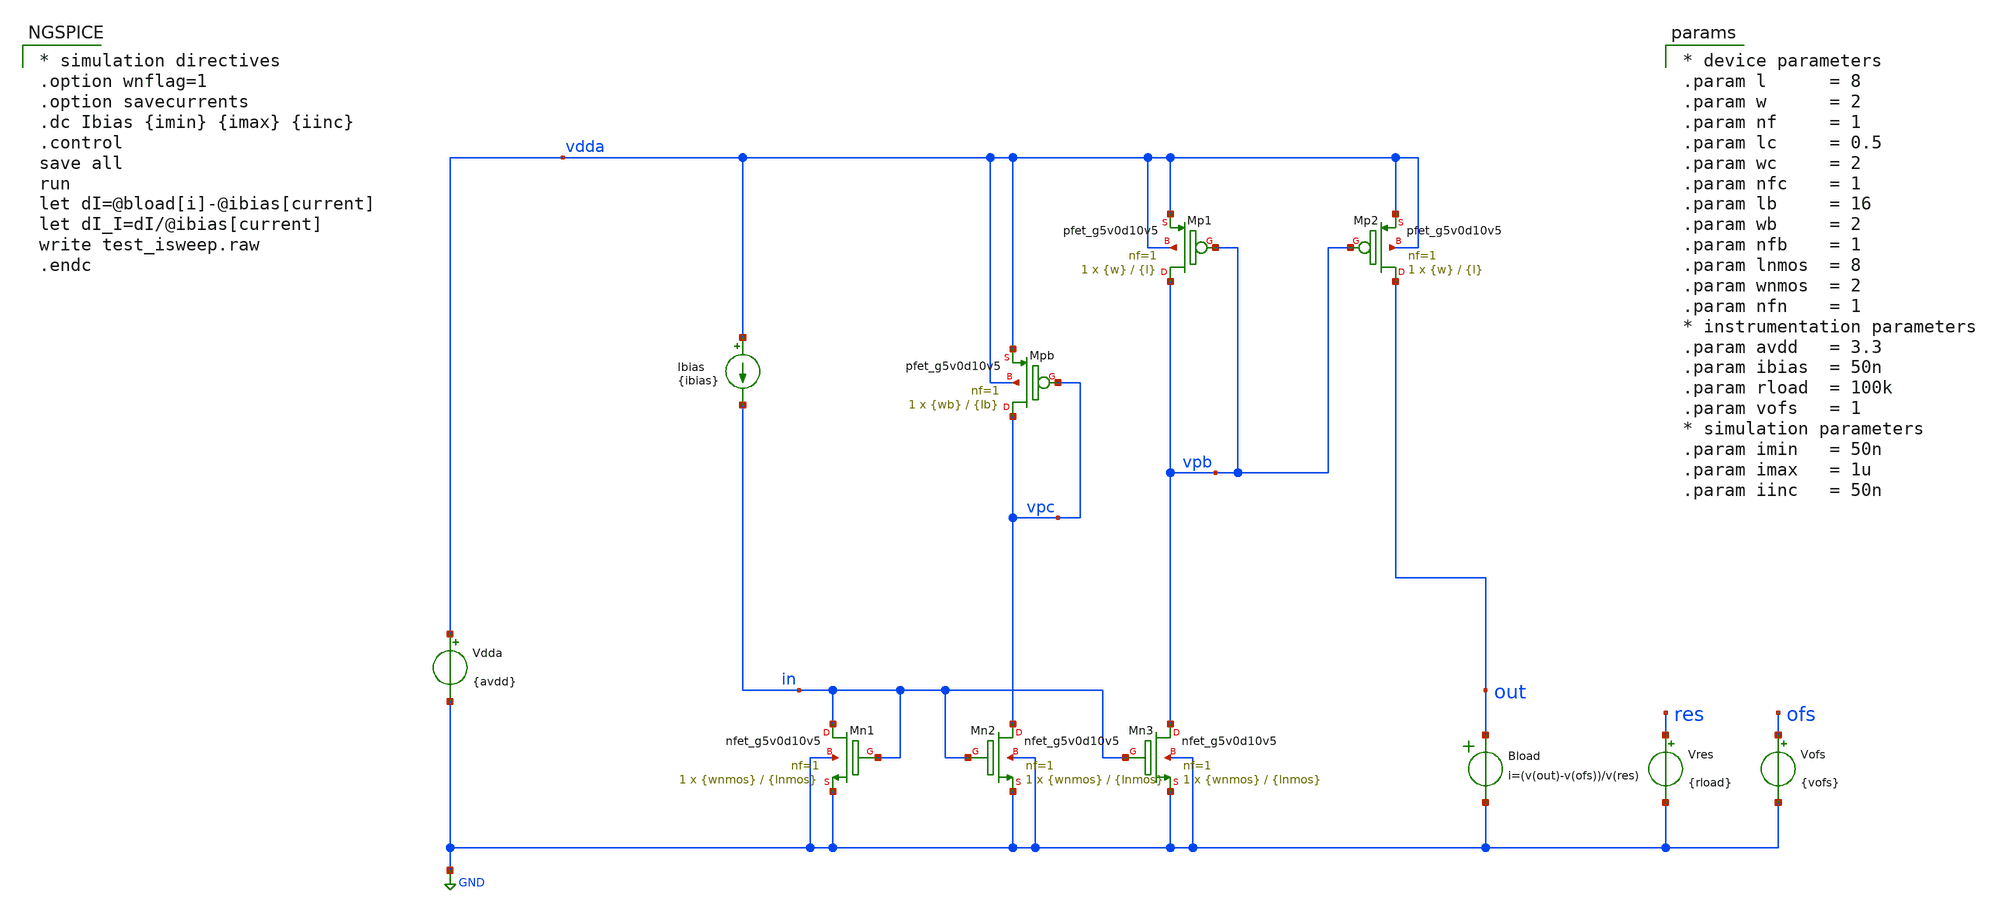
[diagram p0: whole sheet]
** sch_path: xschem/test_isweep.sch
**.subckt test_isweep
Vdda vdda GND {avdd}
.save i(vdda)
Ibias vdda in {ibias}
Vres res GND {rload}
Bload out GND i=(v(out)-v(ofs))/v(res)
Vofs ofs GND {vofs}
XMn1 in in GND GND sky130_fd_pr__nfet_g5v0d10v5 L={lnmos} W={wnmos} nf=1 ad='int((1 + 1)/2) * {wnmos} / 1 * 0.29'
+ as='int((1 + 2)/2) * {wnmos} / 1 * 0.29' pd='2*int((1 + 1)/2) * ({wnmos} / 1 + 0.29)' ps='2*int((1 + 2)/2) * ({wnmos} / 1 + 0.29)'
+ nrd='0.29 / {wnmos} ' nrs='0.29 / {wnmos} ' sa=0 sb=0 sd=0 mult=1 m=1
XMn2 vpc in GND GND sky130_fd_pr__nfet_g5v0d10v5 L={lnmos} W={wnmos} nf=1 ad='int((1 + 1)/2) * {wnmos} / 1 * 0.29'
+ as='int((1 + 2)/2) * {wnmos} / 1 * 0.29' pd='2*int((1 + 1)/2) * ({wnmos} / 1 + 0.29)' ps='2*int((1 + 2)/2) * ({wnmos} / 1 + 0.29)'
+ nrd='0.29 / {wnmos} ' nrs='0.29 / {wnmos} ' sa=0 sb=0 sd=0 mult=1 m=1
XMn3 vpb in GND GND sky130_fd_pr__nfet_g5v0d10v5 L={lnmos} W={wnmos} nf=1 ad='int((1 + 1)/2) * {wnmos} / 1 * 0.29'
+ as='int((1 + 2)/2) * {wnmos} / 1 * 0.29' pd='2*int((1 + 1)/2) * ({wnmos} / 1 + 0.29)' ps='2*int((1 + 2)/2) * ({wnmos} / 1 + 0.29)'
+ nrd='0.29 / {wnmos} ' nrs='0.29 / {wnmos} ' sa=0 sb=0 sd=0 mult=1 m=1
XMpb vpc vpc vdda vdda sky130_fd_pr__pfet_g5v0d10v5 L={lb} W={wb} nf=1 ad='int((1 + 1)/2) * {wb} / 1 * 0.29'
+ as='int((1 + 2)/2) * {wb} / 1 * 0.29' pd='2*int((1 + 1)/2) * ({wb} / 1 + 0.29)' ps='2*int((1 + 2)/2) * ({wb} / 1 + 0.29)'
+ nrd='0.29 / {wb} ' nrs='0.29 / {wb} ' sa=0 sb=0 sd=0 mult=1 m=1
XMp1 vpb vpb vdda vdda sky130_fd_pr__pfet_g5v0d10v5 L={l} W={w} nf=1 ad='int((1 + 1)/2) * {w} / 1 * 0.29'
+ as='int((1 + 2)/2) * {w} / 1 * 0.29' pd='2*int((1 + 1)/2) * ({w} / 1 + 0.29)' ps='2*int((1 + 2)/2) * ({w} / 1 + 0.29)'
+ nrd='0.29 / {w} ' nrs='0.29 / {w} ' sa=0 sb=0 sd=0 mult=1 m=1
XMp2 out vpb vdda vdda sky130_fd_pr__pfet_g5v0d10v5 L={l} W={w} nf=1 ad='int((1 + 1)/2) * {w} / 1 * 0.29'
+ as='int((1 + 2)/2) * {w} / 1 * 0.29' pd='2*int((1 + 1)/2) * ({w} / 1 + 0.29)' ps='2*int((1 + 2)/2) * ({w} / 1 + 0.29)'
+ nrd='0.29 / {w} ' nrs='0.29 / {w} ' sa=0 sb=0 sd=0 mult=1 m=1
**** begin user architecture code

* device parameters
.param l      = 8
.param w      = 2
.param nf     = 1
.param lc     = 0.5
.param wc     = 2
.param nfc    = 1
.param lb     = 16
.param wb     = 2
.param nfb    = 1
.param lnmos  = 8
.param wnmos  = 2
.param nfn    = 1
* instrumentation parameters
.param avdd   = 3.3
.param ibias  = 50n
.param rload  = 100k
.param vofs   = 1
* simulation parameters
.param imin   = 50n
.param imax   = 1u
.param iinc   = 50n


** opencircuitdesign pdks install
.lib $::SKYWATER_MODELS/sky130.lib.spice tt



* simulation directives
.option wnflag=1
.option savecurrents
.dc Ibias {imin} {imax} {iinc}
.control
save all
run
let dI=@bload[i]-@ibias[current]
let dI_I=dI/@ibias[current]
write test_isweep.raw
.endc


**** end user architecture code
**.ends
.GLOBAL GND
.end
